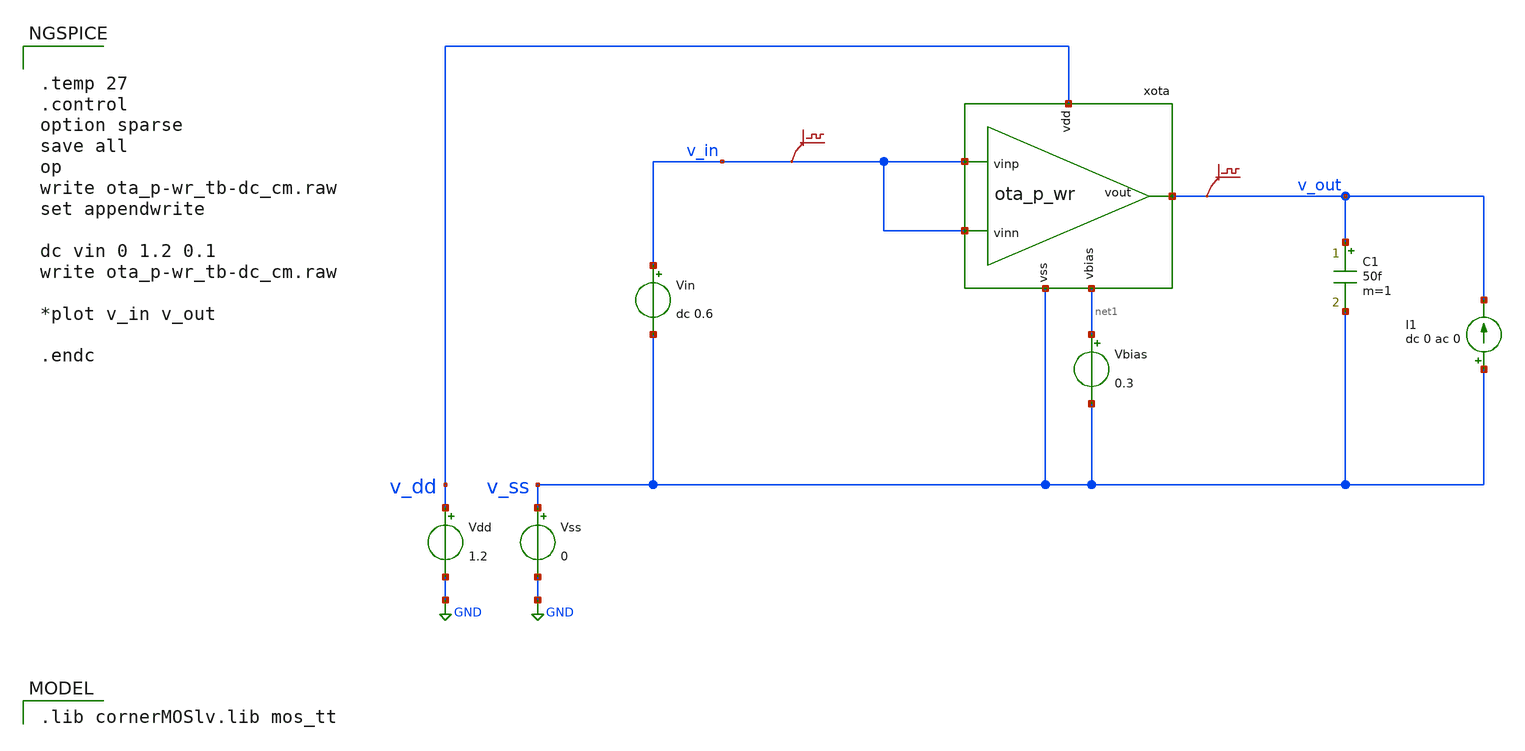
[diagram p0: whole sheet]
** sch_path: v2_feature_extr_withf/ota_p-wr_tb-dc_cm.sch
* (c) 2024-2025 Harald Pretl, Apache-2.0 license
**.subckt ota_p-wr_tb-dc_cm
Vdd v_dd GND 1.2
xota v_dd v_out v_in v_in net1 v_ss ota_p_wr
Vss v_ss GND 0
C1 v_out v_ss 50f m=1
Vin v_in v_ss dc 0.6
.save v(v_in)
.save v(v_out)
I1 v_ss v_out dc 0 ac 0
Vbias net1 v_ss 0.3
**** begin user architecture code
 .lib cornerMOSlv.lib mos_tt



.temp 27
.control
option sparse
save all
op
write ota_p-wr_tb-dc_cm.raw
set appendwrite

dc vin 0 1.2 0.1
write ota_p-wr_tb-dc_cm.raw

*plot v_in v_out

.endc


**** end user architecture code
**.ends
.GLOBAL GND
.end
